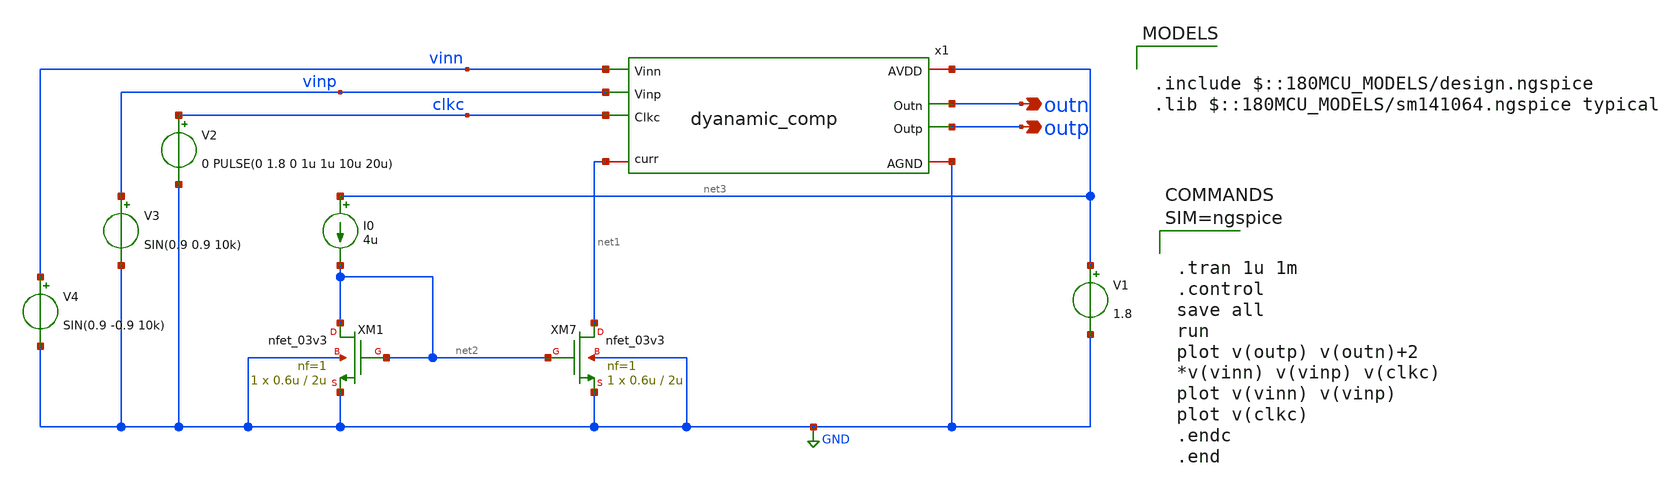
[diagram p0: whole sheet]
** sch_path: xschem/tb_dyanamic_comp.sch
**.subckt tb_dyanamic_comp outn outp
*.opin outn
*.opin outp
XM7 net1 net2 GND GND nfet_03v3 L=2u W=0.6u nf=1 ad='int((nf+1)/2) * W/nf * 0.18u' as='int((nf+2)/2) * W/nf * 0.18u'
+ pd='2*int((nf+1)/2) * (W/nf + 0.18u)' ps='2*int((nf+2)/2) * (W/nf + 0.18u)' nrd='0.18u / W' nrs='0.18u / W'
+ sa=0 sb=0 sd=0 m=1
XM1 net2 net2 GND GND nfet_03v3 L=2u W=0.6u nf=1 ad='int((nf+1)/2) * W/nf * 0.18u' as='int((nf+2)/2) * W/nf * 0.18u'
+ pd='2*int((nf+1)/2) * (W/nf + 0.18u)' ps='2*int((nf+2)/2) * (W/nf + 0.18u)' nrd='0.18u / W' nrs='0.18u / W'
+ sa=0 sb=0 sd=0 m=1
I0 net3 net2 4u
V1 net3 GND 1.8
V2 clkc GND 0 PULSE(0 1.8 0 1u 1u 10u 20u)
V3 vinp GND SIN(0.9 0.9 10k)
V4 vinn GND SIN(0.9 -0.9 10k)
x1 net3 net1 vinn vinp outn outp clkc GND dyanamic_comp
**** begin user architecture code



.tran 1u 1m
.control
save all
run
plot v(outp) v(outn)+2
*v(vinn) v(vinp) v(clkc)
plot v(vinn) v(vinp)
plot v(clkc)
.endc
.end




.include $::180MCU_MODELS/design.ngspice
.lib $::180MCU_MODELS/sm141064.ngspice typical

**** end user architecture code
**.ends

* expanding   symbol:  dyanamic_comp.sym # of pins=8
** sym_path: xschem/dyanamic_comp.sym
** sch_path: xschem/dyanamic_comp.sch
.subckt dyanamic_comp AVDD curr Vinn Vinp Outn Outp Clkc AGND
*.iopin AVDD
*.iopin curr
*.opin Outp
*.ipin Clkc
*.iopin AGND
*.opin Outn
*.ipin Vinp
*.ipin Vinn
XMP1 net5 Vinp net2 AVDD pfet_03v3 L=2u W=2u nf=1 ad='int((nf+1)/2) * W/nf * 0.18u' as='int((nf+2)/2) * W/nf * 0.18u'
+ pd='2*int((nf+1)/2) * (W/nf + 0.18u)' ps='2*int((nf+2)/2) * (W/nf + 0.18u)' nrd='0.18u / W' nrs='0.18u / W'
+ sa=0 sb=0 sd=0 m=9
XMP2 net6 Vinn net2 AVDD pfet_03v3 L=2u W=2u nf=1 ad='int((nf+1)/2) * W/nf * 0.18u' as='int((nf+2)/2) * W/nf * 0.18u'
+ pd='2*int((nf+1)/2) * (W/nf + 0.18u)' ps='2*int((nf+2)/2) * (W/nf + 0.18u)' nrd='0.18u / W' nrs='0.18u / W'
+ sa=0 sb=0 sd=0 m=9
XMN4 net6 net3 AGND AGND nfet_03v3 L=2u W=0.6u nf=1 ad='int((nf+1)/2) * W/nf * 0.18u' as='int((nf+2)/2) * W/nf * 0.18u'
+ pd='2*int((nf+1)/2) * (W/nf + 0.18u)' ps='2*int((nf+2)/2) * (W/nf + 0.18u)' nrd='0.18u / W' nrs='0.18u / W'
+ sa=0 sb=0 sd=0 m=1
XMN5 net3 Clkc AGND AGND nfet_03v3 L=2u W=0.6u nf=1 ad='int((nf+1)/2) * W/nf * 0.18u' as='int((nf+2)/2) * W/nf * 0.18u'
+ pd='2*int((nf+1)/2) * (W/nf + 0.18u)' ps='2*int((nf+2)/2) * (W/nf + 0.18u)' nrd='0.18u / W' nrs='0.18u / W'
+ sa=0 sb=0 sd=0 m=1
XMN6 net4 Clkc AGND AGND nfet_03v3 L=2u W=0.6u nf=1 ad='int((nf+1)/2) * W/nf * 0.18u' as='int((nf+2)/2) * W/nf * 0.18u'
+ pd='2*int((nf+1)/2) * (W/nf + 0.18u)' ps='2*int((nf+2)/2) * (W/nf + 0.18u)' nrd='0.18u / W' nrs='0.18u / W'
+ sa=0 sb=0 sd=0 m=1
XMN3 net5 net4 AGND AGND nfet_03v3 L=2u W=0.6u nf=1 ad='int((nf+1)/2) * W/nf * 0.18u' as='int((nf+2)/2) * W/nf * 0.18u'
+ pd='2*int((nf+1)/2) * (W/nf + 0.18u)' ps='2*int((nf+2)/2) * (W/nf + 0.18u)' nrd='0.18u / W' nrs='0.18u / W'
+ sa=0 sb=0 sd=0 m=1
XMP7 net2 Clkc net1 AVDD pfet_03v3 L=2u W=1.12u nf=1 ad='int((nf+1)/2) * W/nf * 0.18u' as='int((nf+2)/2) * W/nf * 0.18u'
+ pd='2*int((nf+1)/2) * (W/nf + 0.18u)' ps='2*int((nf+2)/2) * (W/nf + 0.18u)' nrd='0.18u / W' nrs='0.18u / W'
+ sa=0 sb=0 sd=0 m=1
XMPB net1 curr AVDD AVDD pfet_03v3 L=2u W=1.12u nf=1 ad='int((nf+1)/2) * W/nf * 0.18u' as='int((nf+2)/2) * W/nf * 0.18u'
+ pd='2*int((nf+1)/2) * (W/nf + 0.18u)' ps='2*int((nf+2)/2) * (W/nf + 0.18u)' nrd='0.18u / W' nrs='0.18u / W'
+ sa=0 sb=0 sd=0 m=1
XMP12 curr curr AVDD AVDD pfet_03v3 L=2u W=1.12u nf=1 ad='int((nf+1)/2) * W/nf * 0.18u' as='int((nf+2)/2) * W/nf * 0.18u'
+ pd='2*int((nf+1)/2) * (W/nf + 0.18u)' ps='2*int((nf+2)/2) * (W/nf + 0.18u)' nrd='0.18u / W' nrs='0.18u / W'
+ sa=0 sb=0 sd=0 m=1
XMP10 Outn net7 AVDD AVDD pfet_03v3 L=2u W=1.12u nf=1 ad='int((nf+1)/2) * W/nf * 0.18u' as='int((nf+2)/2) * W/nf * 0.18u'
+ pd='2*int((nf+1)/2) * (W/nf + 0.18u)' ps='2*int((nf+2)/2) * (W/nf + 0.18u)' nrd='0.18u / W' nrs='0.18u / W'
+ sa=0 sb=0 sd=0 m=1
XMN11 Outn net7 AGND AGND nfet_03v3 L=2u W=0.6u nf=1 ad='int((nf+1)/2) * W/nf * 0.18u' as='int((nf+2)/2) * W/nf * 0.18u'
+ pd='2*int((nf+1)/2) * (W/nf + 0.18u)' ps='2*int((nf+2)/2) * (W/nf + 0.18u)' nrd='0.18u / W' nrs='0.18u / W'
+ sa=0 sb=0 sd=0 m=1
XMP8 Outp net3 AVDD AVDD pfet_03v3 L=2u W=1.12u nf=1 ad='int((nf+1)/2) * W/nf * 0.18u' as='int((nf+2)/2) * W/nf * 0.18u'
+ pd='2*int((nf+1)/2) * (W/nf + 0.18u)' ps='2*int((nf+2)/2) * (W/nf + 0.18u)' nrd='0.18u / W' nrs='0.18u / W'
+ sa=0 sb=0 sd=0 m=1
XMN9 Outp net3 AGND AGND nfet_03v3 L=2u W=0.6u nf=1 ad='int((nf+1)/2) * W/nf * 0.18u' as='int((nf+2)/2) * W/nf * 0.18u'
+ pd='2*int((nf+1)/2) * (W/nf + 0.18u)' ps='2*int((nf+2)/2) * (W/nf + 0.18u)' nrd='0.18u / W' nrs='0.18u / W'
+ sa=0 sb=0 sd=0 m=1
V1 net4 net7 0
.ends

.GLOBAL GND
.end
